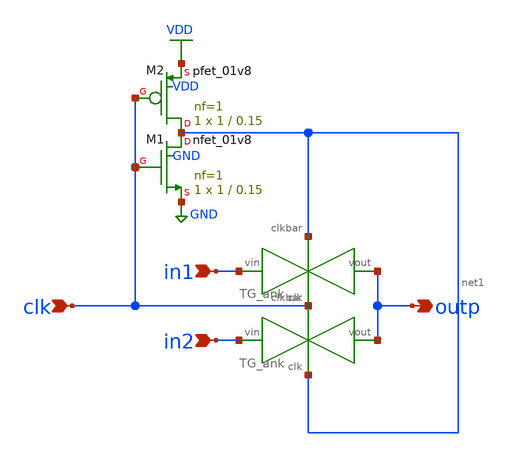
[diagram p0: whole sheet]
** sch_path: xschem/comparator/mux21_ank.sch
**.subckt mux21_ank in1 in2 clk outp
*.ipin in1
*.ipin in2
*.ipin clk
*.opin outp
XM1 net1 clk GND GND sky130_fd_pr__nfet_01v8 L=0.15 W=1 nf=1 ad='int((nf+1)/2) * W/nf * 0.29' as='int((nf+2)/2) * W/nf * 0.29'
+ pd='2*int((nf+1)/2) * (W/nf + 0.29)' ps='2*int((nf+2)/2) * (W/nf + 0.29)' nrd='0.29 / W' nrs='0.29 / W'
+ sa=0 sb=0 sd=0 mult=1 m=1
XM2 net1 clk VDD VDD sky130_fd_pr__pfet_01v8 L=0.15 W=1 nf=1 ad='int((nf+1)/2) * W/nf * 0.29' as='int((nf+2)/2) * W/nf * 0.29'
+ pd='2*int((nf+1)/2) * (W/nf + 0.29)' ps='2*int((nf+2)/2) * (W/nf + 0.29)' nrd='0.29 / W' nrs='0.29 / W'
+ sa=0 sb=0 sd=0 mult=1 m=1
x1 in1 net1 clk outp TG_ank
x1 in2 clk net1 outp TG_ank
**.ends

* expanding   symbol:  /home/sky/fossi_cochlea/xschem/comparator/TG_ank.sym # of pins=4
** sym_path: xschem/comparator/TG_ank.sym
** sch_path: xschem/comparator/TG_ank.sch
.subckt TG_ank vin clkbar clk vout
*.ipin clkbar
*.opin vout
*.ipin vin
*.ipin clk
XM1 vout clk vin GND sky130_fd_pr__nfet_01v8 L=0.15 W=1 nf=1 ad='int((nf+1)/2) * W/nf * 0.29' as='int((nf+2)/2) * W/nf * 0.29'
+ pd='2*int((nf+1)/2) * (W/nf + 0.29)' ps='2*int((nf+2)/2) * (W/nf + 0.29)' nrd='0.29 / W' nrs='0.29 / W'
+ sa=0 sb=0 sd=0 mult=1 m=1
XM2 vout clkbar vin VDD sky130_fd_pr__pfet_01v8 L=0.15 W=1 nf=1 ad='int((nf+1)/2) * W/nf * 0.29' as='int((nf+2)/2) * W/nf * 0.29'
+ pd='2*int((nf+1)/2) * (W/nf + 0.29)' ps='2*int((nf+2)/2) * (W/nf + 0.29)' nrd='0.29 / W' nrs='0.29 / W'
+ sa=0 sb=0 sd=0 mult=1 m=1
.ends

.GLOBAL GND
.GLOBAL VDD
.end
